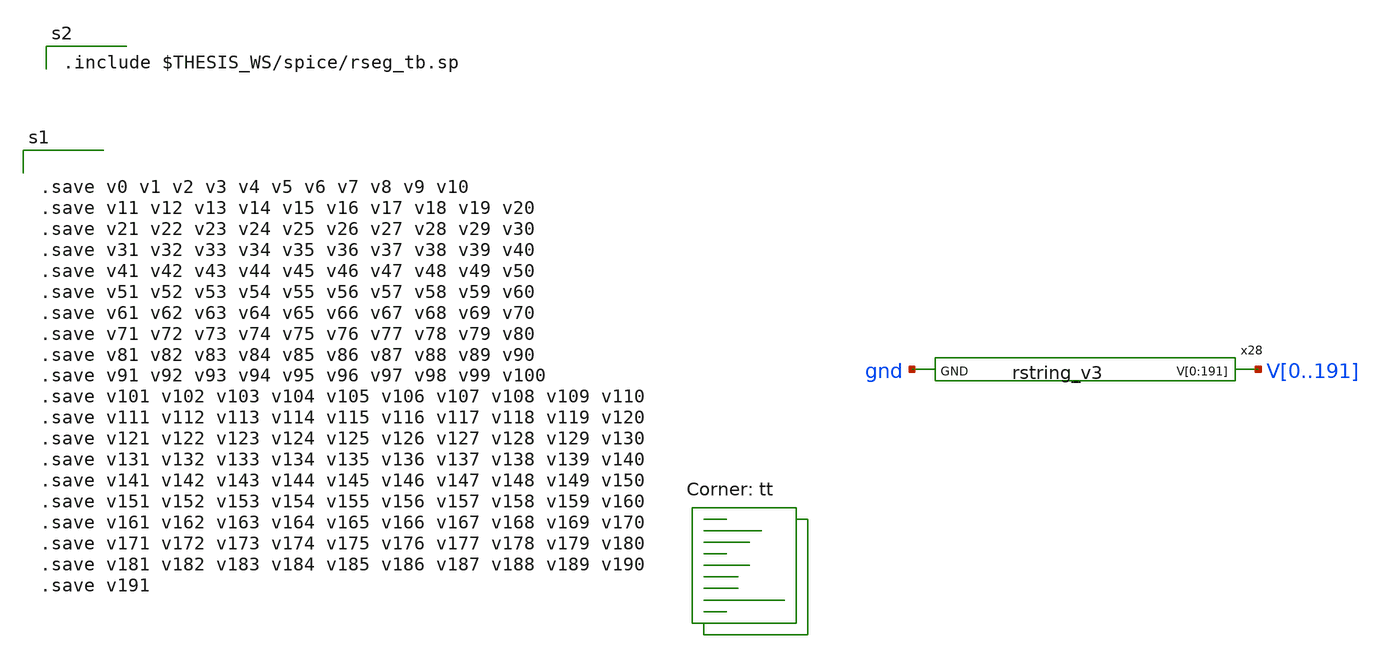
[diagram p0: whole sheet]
** sch_path: xschem/res_seg-tb.sch
**.subckt res_seg-tb
x28 V0 V1 V2 V3 V4 V5 V6 V7 V8 V9 V10 V11 V12 V13 V14 V15 V16 V17 V18 V19 V20 V21 V22 V23 V24 V25
+ V26 V27 V28 V29 V30 V31 V32 V33 V34 V35 V36 V37 V38 V39 V40 V41 V42 V43 V44 V45 V46 V47 V48 V49 V50 V51
+ V52 V53 V54 V55 V56 V57 V58 V59 V60 V61 V62 V63 V64 V65 V66 V67 V68 V69 V70 V71 V72 V73 V74 V75 V76 V77
+ V78 V79 V80 V81 V82 V83 V84 V85 V86 V87 V88 V89 V90 V91 V92 V93 V94 V95 V96 V97 V98 V99 V100 V101 V102
+ V103 V104 V105 V106 V107 V108 V109 V110 V111 V112 V113 V114 V115 V116 V117 V118 V119 V120 V121 V122 V123
+ V124 V125 V126 V127 V128 V129 V130 V131 V132 V133 V134 V135 V136 V137 V138 V139 V140 V141 V142 V143 V144
+ V145 V146 V147 V148 V149 V150 V151 V152 V153 V154 V155 V156 V157 V158 V159 V160 V161 V162 V163 V164 V165
+ V166 V167 V168 V169 V170 V171 V172 V173 V174 V175 V176 V177 V178 V179 V180 V181 V182 V183 V184 V185 V186
+ V187 V188 V189 V190 V191 gnd rstring_v3
**** begin user architecture code
.lib $::SKYWATER_MODELS/sky130.lib.spice tt


.save v0 v1 v2 v3 v4 v5 v6 v7 v8 v9 v10
.save v11 v12 v13 v14 v15 v16 v17 v18 v19 v20
.save v21 v22 v23 v24 v25 v26 v27 v28 v29 v30
.save v31 v32 v33 v34 v35 v36 v37 v38 v39 v40
.save v41 v42 v43 v44 v45 v46 v47 v48 v49 v50
.save v51 v52 v53 v54 v55 v56 v57 v58 v59 v60
.save v61 v62 v63 v64 v65 v66 v67 v68 v69 v70
.save v71 v72 v73 v74 v75 v76 v77 v78 v79 v80
.save v81 v82 v83 v84 v85 v86 v87 v88 v89 v90
.save v91 v92 v93 v94 v95 v96 v97 v98 v99 v100
.save v101 v102 v103 v104 v105 v106 v107 v108 v109 v110
.save v111 v112 v113 v114 v115 v116 v117 v118 v119 v120
.save v121 v122 v123 v124 v125 v126 v127 v128 v129 v130
.save v131 v132 v133 v134 v135 v136 v137 v138 v139 v140
.save v141 v142 v143 v144 v145 v146 v147 v148 v149 v150
.save v151 v152 v153 v154 v155 v156 v157 v158 v159 v160
.save v161 v162 v163 v164 v165 v166 v167 v168 v169 v170
.save v171 v172 v173 v174 v175 v176 v177 v178 v179 v180
.save v181 v182 v183 v184 v185 v186 v187 v188 v189 v190
.save v191



.include $THESIS_WS/spice/rseg_tb.sp

**** end user architecture code
**.ends

* expanding   symbol:  rstring_v3.sym # of pins=2
** sym_path: xschem/rstring_v3.sym
** sch_path: xschem/rstring_v3.sch
.subckt rstring_v3 V[0] V[1] V[2] V[3] V[4] V[5] V[6] V[7] V[8] V[9] V[10] V[11] V[12] V[13] V[14]
+ V[15] V[16] V[17] V[18] V[19] V[20] V[21] V[22] V[23] V[24] V[25] V[26] V[27] V[28] V[29] V[30] V[31]
+ V[32] V[33] V[34] V[35] V[36] V[37] V[38] V[39] V[40] V[41] V[42] V[43] V[44] V[45] V[46] V[47] V[48]
+ V[49] V[50] V[51] V[52] V[53] V[54] V[55] V[56] V[57] V[58] V[59] V[60] V[61] V[62] V[63] V[64] V[65]
+ V[66] V[67] V[68] V[69] V[70] V[71] V[72] V[73] V[74] V[75] V[76] V[77] V[78] V[79] V[80] V[81] V[82]
+ V[83] V[84] V[85] V[86] V[87] V[88] V[89] V[90] V[91] V[92] V[93] V[94] V[95] V[96] V[97] V[98] V[99]
+ V[100] V[101] V[102] V[103] V[104] V[105] V[106] V[107] V[108] V[109] V[110] V[111] V[112] V[113] V[114]
+ V[115] V[116] V[117] V[118] V[119] V[120] V[121] V[122] V[123] V[124] V[125] V[126] V[127] V[128] V[129]
+ V[130] V[131] V[132] V[133] V[134] V[135] V[136] V[137] V[138] V[139] V[140] V[141] V[142] V[143] V[144]
+ V[145] V[146] V[147] V[148] V[149] V[150] V[151] V[152] V[153] V[154] V[155] V[156] V[157] V[158] V[159]
+ V[160] V[161] V[162] V[163] V[164] V[165] V[166] V[167] V[168] V[169] V[170] V[171] V[172] V[173] V[174]
+ V[175] V[176] V[177] V[178] V[179] V[180] V[181] V[182] V[183] V[184] V[185] V[186] V[187] V[188] V[189]
+ V[190] V[191] GND
*.opin
*+ V[0],V[1],V[2],V[3],V[4],V[5],V[6],V[7],V[8],V[9],V[10],V[11],V[12],V[13],V[14],V[15],V[16],V[17],V[18],V[19],V[20],V[21],V[22],V[23],V[24],V[25],V[26],V[27],V[28],V[29],V[30],V[31],V[32],V[33],V[34],V[35],V[36],V[37],V[38],V[39],V[40],V[41],V[42],V[43],V[44],V[45],V[46],V[47],V[48],V[49],V[50],V[51],V[52],V[53],V[54],V[55],V[56],V[57],V[58],V[59],V[60],V[61],V[62],V[63],V[64],V[65],V[66],V[67],V[68],V[69],V[70],V[71],V[72],V[73],V[74],V[75],V[76],V[77],V[78],V[79],V[80],V[81],V[82],V[83],V[84],V[85],V[86],V[87],V[88],V[89],V[90],V[91],V[92],V[93],V[94],V[95],V[96],V[97],V[98],V[99],V[100],V[101],V[102],V[103],V[104],V[105],V[106],V[107],V[108],V[109],V[110],V[111],V[112],V[113],V[114],V[115],V[116],V[117],V[118],V[119],V[120],V[121],V[122],V[123],V[124],V[125],V[126],V[127],V[128],V[129],V[130],V[131],V[132],V[133],V[134],V[135],V[136],V[137],V[138],V[139],V[140],V[141],V[142],V[143],V[144],V[145],V[146],V[147],V[148],V[149],V[150],V[151],V[152],V[153],V[154],V[155],V[156],V[157],V[158],V[159],V[160],V[161],V[162],V[163],V[164],V[165],V[166],V[167],V[168],V[169],V[170],V[171],V[172],V[173],V[174],V[175],V[176],V[177],V[178],V[179],V[180],V[181],V[182],V[183],V[184],V[185],V[186],V[187],V[188],V[189],V[190],V[191]
*.ipin GND
x1 V[0] V[1] V[2] V[3] V[4] V[5] V[6] V[7] V[8] V[9] V[10] V[11] V[12] V[13] V[14] V[15] V[16] V[17]
+ V[18] V[19] V[20] V[21] V[22] V[23] V[24] V[25] V[26] V[27] V[28] V[29] V[30] V[31] V[32] V[33] V[34]
+ V[35] V[36] V[37] V[38] V[39] V[40] V[41] V[42] V[43] V[44] V[45] V[46] V[47] V[48] V[49] V[50] V[51]
+ V[52] V[53] V[54] V[55] V[56] V[57] V[58] V[59] V[60] V[61] V[62] V[63] V[64] GND rseg_1_v3
x2 V[64] V[65] V[66] V[67] V[68] V[69] V[70] V[71] V[72] V[73] V[74] V[75] V[76] V[77] V[78] V[79]
+ V[80] V[81] V[82] V[83] V[84] V[85] V[86] V[87] V[88] V[89] V[90] V[91] V[92] V[93] V[94] V[95] V[96]
+ V[97] V[98] V[99] V[100] V[101] V[102] V[103] V[104] V[105] V[106] V[107] V[108] V[109] V[110] V[111]
+ V[112] GND rseg_2_v3
x3 V[112] V[113] V[114] V[115] V[116] V[117] V[118] V[119] V[120] V[121] V[122] V[123] V[124] V[125]
+ V[126] V[127] V[128] GND rseg_3_v3
x4 V[128] V[129] V[130] V[131] V[132] V[133] V[134] V[135] V[136] V[137] V[138] V[139] V[140] V[141]
+ V[142] V[143] V[144] V[145] V[146] V[147] V[148] V[149] V[150] V[151] V[152] V[153] V[154] V[155] V[156]
+ V[157] V[158] V[159] V[160] V[161] V[162] V[163] V[164] V[165] V[166] V[167] V[168] V[169] V[170] V[171]
+ V[172] V[173] V[174] V[175] V[176] V[177] V[178] V[179] V[180] V[181] V[182] V[183] V[184] V[185] V[186]
+ V[187] V[188] V[189] V[190] V[191] GND rseg_4_v3
.ends

.end
